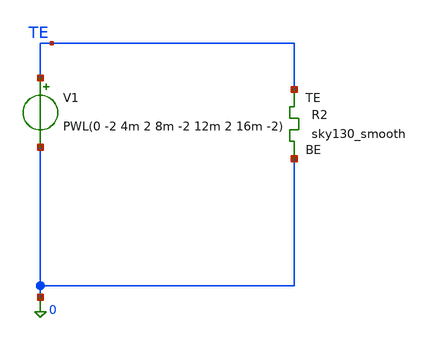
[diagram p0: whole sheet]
** sch_path: memristor_models/sky130_smooth/tb_liss_smooth.sch
**.subckt tb_liss_smooth
V1 TE 0 PWL(0 -2 4m 2 8m -2 12m 2 16m -2)
XR2 TE 0 sky130_smooth Tfilament_0=3.3e-9
**** begin user architecture code

** opencircuitdesign pdks install
.inc $::SKYWATER_MODELS/sky130_smooth.spice



.option savecurrents
.tran 1u 16m
.control
	save all
	run
	write tb_liss_smooth.raw
.endc



**** end user architecture code
**.ends
.end
